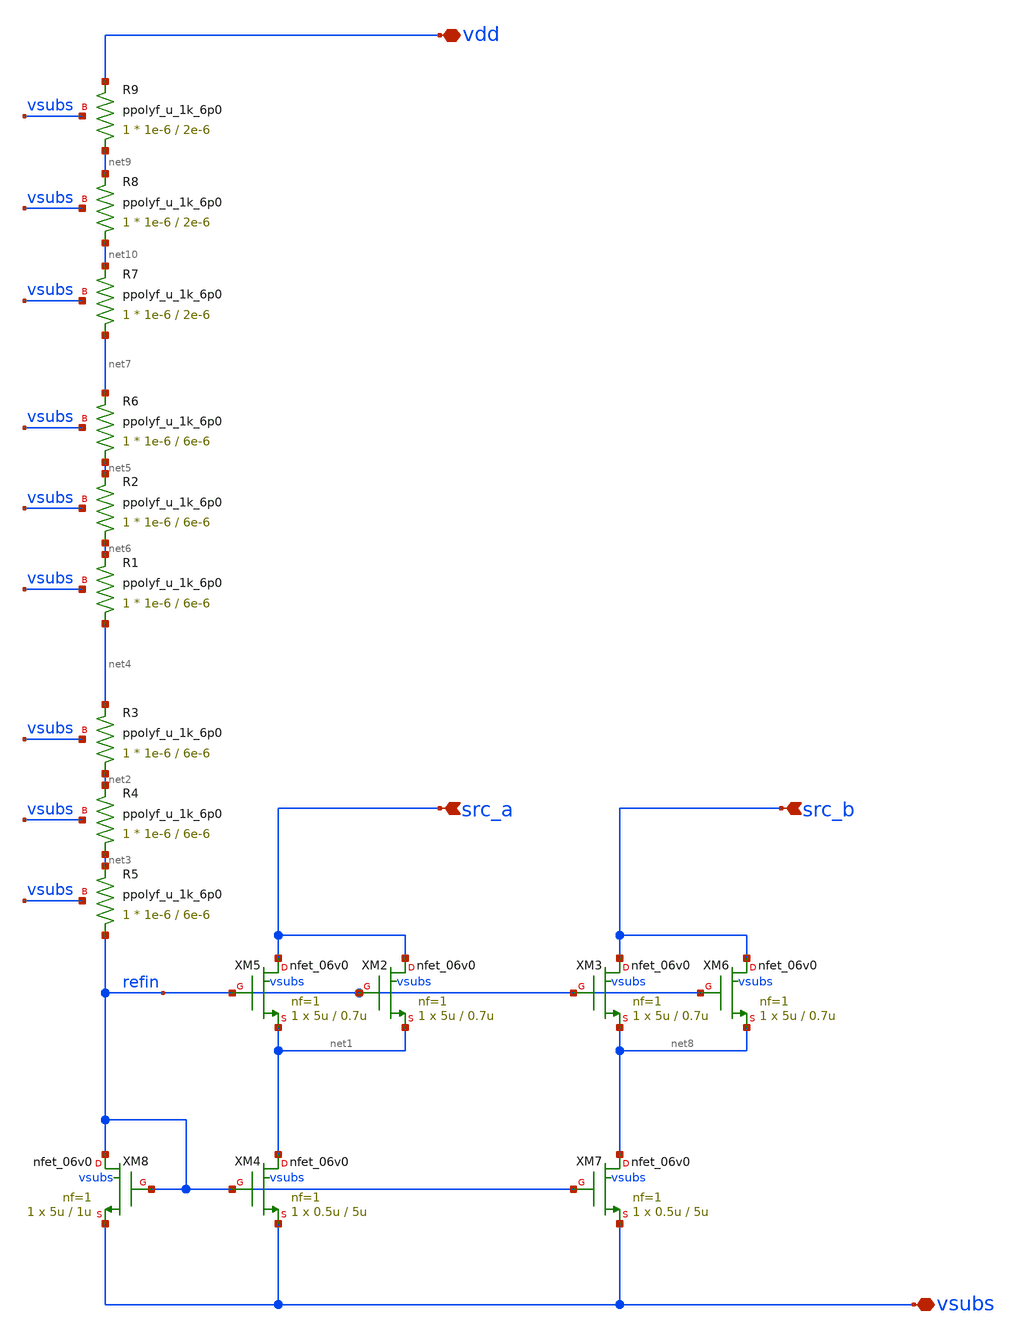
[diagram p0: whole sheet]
** sch_path: xschem/ip_current_source.sch
**.subckt ip_current_source vdd vsubs src_a src_b
*.iopin vdd
*.iopin vsubs
*.ipin src_a
*.ipin src_b
XM8 refin refin vsubs vsubs nfet_06v0 L=1u W=5u nf=1 ad='int((nf+1)/2) * W/nf * 0.18u' as='int((nf+2)/2) * W/nf * 0.18u'
+ pd='2*int((nf+1)/2) * (W/nf + 0.18u)' ps='2*int((nf+2)/2) * (W/nf + 0.18u)' nrd='0.18u / W' nrs='0.18u / W'
+ sa=0 sb=0 sd=0 m=1 par=1
XM5 src_a refin net1 vsubs nfet_06v0 L=0.7u W=5u nf=1 ad='int((nf+1)/2) * W/nf * 0.18u' as='int((nf+2)/2) * W/nf * 0.18u'
+ pd='2*int((nf+1)/2) * (W/nf + 0.18u)' ps='2*int((nf+2)/2) * (W/nf + 0.18u)' nrd='0.18u / W' nrs='0.18u / W'
+ sa=0 sb=0 sd=0 m=1 par=1
XM2 src_a refin net1 vsubs nfet_06v0 L=0.7u W=5u nf=1 ad='int((nf+1)/2) * W/nf * 0.18u' as='int((nf+2)/2) * W/nf * 0.18u'
+ pd='2*int((nf+1)/2) * (W/nf + 0.18u)' ps='2*int((nf+2)/2) * (W/nf + 0.18u)' nrd='0.18u / W' nrs='0.18u / W'
+ sa=0 sb=0 sd=0 m=1 par=1
XM3 src_b refin net8 vsubs nfet_06v0 L=0.7u W=5u nf=1 ad='int((nf+1)/2) * W/nf * 0.18u' as='int((nf+2)/2) * W/nf * 0.18u'
+ pd='2*int((nf+1)/2) * (W/nf + 0.18u)' ps='2*int((nf+2)/2) * (W/nf + 0.18u)' nrd='0.18u / W' nrs='0.18u / W'
+ sa=0 sb=0 sd=0 m=1 par=1
XM6 src_b refin net8 vsubs nfet_06v0 L=0.7u W=5u nf=1 ad='int((nf+1)/2) * W/nf * 0.18u' as='int((nf+2)/2) * W/nf * 0.18u'
+ pd='2*int((nf+1)/2) * (W/nf + 0.18u)' ps='2*int((nf+2)/2) * (W/nf + 0.18u)' nrd='0.18u / W' nrs='0.18u / W'
+ sa=0 sb=0 sd=0 m=1 par=1
XM4 net1 refin vsubs vsubs nfet_06v0 L=5u W=0.5u nf=1 ad='int((nf+1)/2) * W/nf * 0.18u' as='int((nf+2)/2) * W/nf * 0.18u'
+ pd='2*int((nf+1)/2) * (W/nf + 0.18u)' ps='2*int((nf+2)/2) * (W/nf + 0.18u)' nrd='0.18u / W' nrs='0.18u / W'
+ sa=0 sb=0 sd=0 m=1 par=1
XM7 net8 refin vsubs vsubs nfet_06v0 L=5u W=0.5u nf=1 ad='int((nf+1)/2) * W/nf * 0.18u' as='int((nf+2)/2) * W/nf * 0.18u'
+ pd='2*int((nf+1)/2) * (W/nf + 0.18u)' ps='2*int((nf+2)/2) * (W/nf + 0.18u)' nrd='0.18u / W' nrs='0.18u / W'
+ sa=0 sb=0 sd=0 m=1 par=1
XR3 net2 net4 vsubs ppolyf_u_1k_6p0 r_width=1e-6 r_length=6e-6 m=1
XR4 net3 net2 vsubs ppolyf_u_1k_6p0 r_width=1e-6 r_length=6e-6 m=1
XR5 refin net3 vsubs ppolyf_u_1k_6p0 r_width=1e-6 r_length=6e-6 m=1
XR1 net4 net6 vsubs ppolyf_u_1k_6p0 r_width=1e-6 r_length=6e-6 m=1
XR2 net6 net5 vsubs ppolyf_u_1k_6p0 r_width=1e-6 r_length=6e-6 m=1
XR6 net5 net7 vsubs ppolyf_u_1k_6p0 r_width=1e-6 r_length=6e-6 m=1
XR7 net7 net10 vsubs ppolyf_u_1k_6p0 r_width=1e-6 r_length=2e-6 m=1
XR8 net10 net9 vsubs ppolyf_u_1k_6p0 r_width=1e-6 r_length=2e-6 m=1
XR9 net9 vdd vsubs ppolyf_u_1k_6p0 r_width=1e-6 r_length=2e-6 m=1
**.ends
.end
